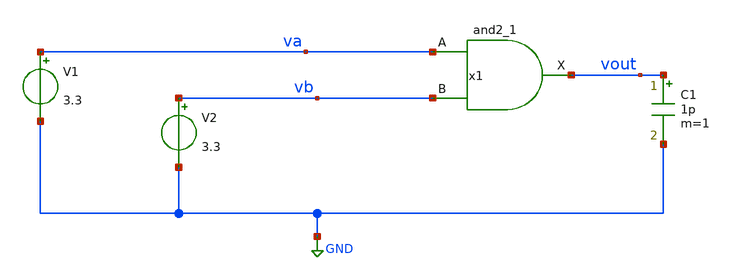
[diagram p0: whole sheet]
** sch_path: xschem/stdcell3tb.sch
**.subckt stdcell3tb
x1 va vb GND GND va va vout sky130_fd_sc_hvl__and2_1
V1 va GND 3.3
V2 vb GND 3.3
C1 vout GND 1p m=1
**** begin user architecture code
 .lib $::SKYWATER_MODELS/sky130.lib.spice tt
.include $::SKYWATER_STDCELLS/../../sky130_fd_sc_hvl/spice/sky130_fd_sc_hvl.spice

.param mc_mm_switch=0
.param mc_pr_switch=1



.option wnflag=0
.option savecurrents
.control
save all
dc v2 0 3.3 0.01
plot v(va) v(vb) v(vout)
op
.endc


**** end user architecture code
**.ends
.GLOBAL GND
.end
